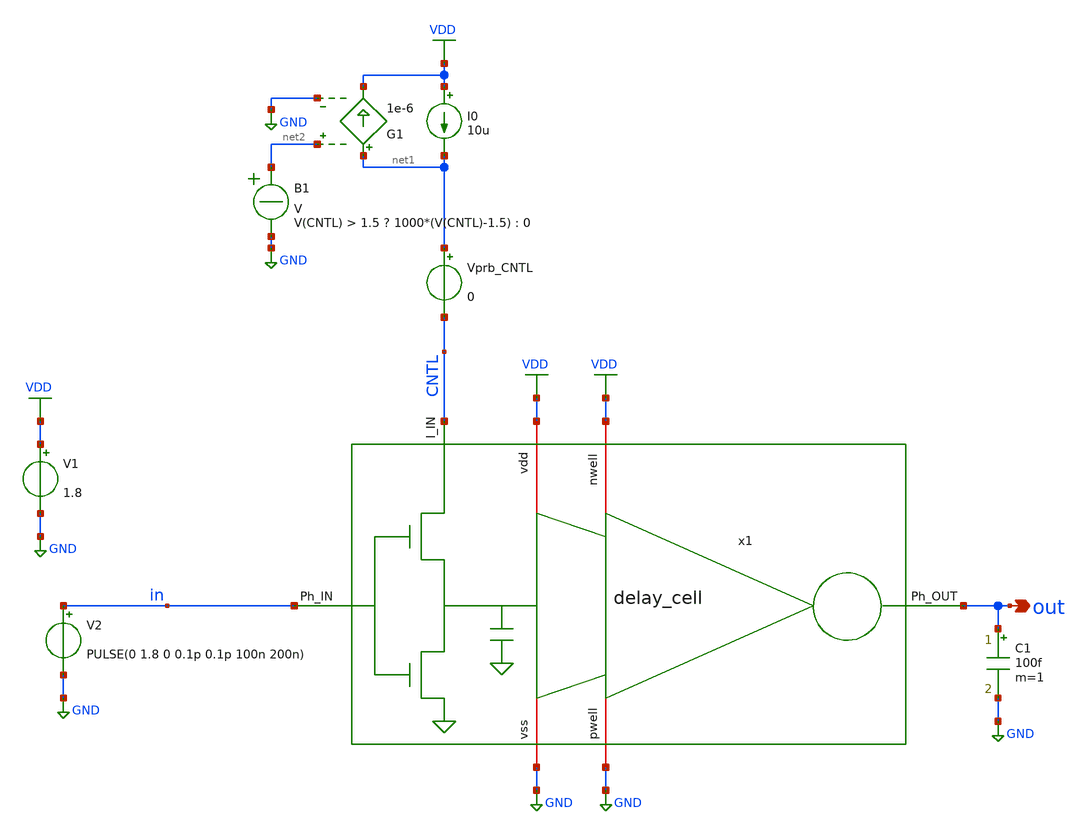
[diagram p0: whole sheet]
** sch_path: design/test/delaycell_test.sch
**.subckt delaycell_test out
*.opin out
V1 VDD GND 1.8
V2 in GND PULSE(0 1.8 0 0.1p 0.1p 100n 200n)
C1 out GND 100f m=1
I0 VDD net1 10u
x1 CNTL VDD VDD GND GND in out delay_cell
G1 net1 VDD net2 GND 1e-6
B1 net2 GND V = V(CNTL) > 1.5 ? 1000*(V(CNTL)-1.5) : 0
Vprb_CNTL net1 CNTL 0
**** begin user architecture code


.param temp=27



*.op
*.ac dec 10 1 10G
*.tran 0.01n 5u


.save all




.options wnflag=1
.include $::SKYWATER_MODELS/cells/nfet_01v8/sky130_fd_pr__nfet_01v8__tt.corner.spice
.include $::SKYWATER_MODELS/cells/nfet_01v8_lvt/sky130_fd_pr__nfet_01v8_lvt__tt.corner.spice
.include $::SKYWATER_MODELS/cells/pfet_01v8/sky130_fd_pr__pfet_01v8__tt.corner.spice
*.include $::SKYWATER_MODELS/cells/nfet_03v3_nvt/sky130_fd_pr__nfet_03v3_nvt__tt.corner.spice
*.include $::SKYWATER_MODELS/cells/nfet_05v0_nvt/sky130_fd_pr__nfet_05v0_nvt__tt.corner.spice
.include $::SKYWATER_MODELS/cells/esd_nfet_01v8/sky130_fd_pr__esd_nfet_01v8__tt.corner.spice
.include $::SKYWATER_MODELS/cells/pfet_01v8_lvt/sky130_fd_pr__pfet_01v8_lvt__tt.corner.spice
*.include $::SKYWATER_MODELS/cells/pfet_01v8_hvt/sky130_fd_pr__pfet_01v8_hvt__tt.corner.spice
*.include $::SKYWATER_MODELS/cells/esd_pfet_g5v0d10v5/sky130_fd_pr__esd_pfet_g5v0d10v5__tt.corner.spice
*.include $::SKYWATER_MODELS/cells/pfet_g5v0d10v5/sky130_fd_pr__pfet_g5v0d10v5__tt.corner.spice
*.include $::SKYWATER_MODELS/cells/pfet_g5v0d16v0/sky130_fd_pr__pfet_g5v0d16v0__tt.corner.spice
*.include $::SKYWATER_MODELS/cells/nfet_g5v0d10v5/sky130_fd_pr__nfet_g5v0d10v5__tt.corner.spice
*.include $::SKYWATER_MODELS/cells/nfet_g5v0d16v0/sky130_fd_pr__nfet_g5v0d16v0__tt_discrete.corner.spice
*.include $::SKYWATER_MODELS/cells/esd_nfet_g5v0d10v5/sky130_fd_pr__esd_nfet_g5v0d10v5__tt.corner.spice
.include $::SKYWATER_MODELS/models/corners/tt/nonfet.spice
* Mismatch parameters
.include $::SKYWATER_MODELS/cells/nfet_01v8/sky130_fd_pr__nfet_01v8__mismatch.corner.spice
.include $::SKYWATER_MODELS/cells/pfet_01v8/sky130_fd_pr__pfet_01v8__mismatch.corner.spice
.include $::SKYWATER_MODELS/cells/nfet_01v8_lvt/sky130_fd_pr__nfet_01v8_lvt__mismatch.corner.spice
.include $::SKYWATER_MODELS/cells/pfet_01v8_lvt/sky130_fd_pr__pfet_01v8_lvt__mismatch.corner.spice
*.include $::SKYWATER_MODELS/cells/pfet_01v8_hvt/sky130_fd_pr__pfet_01v8_hvt__mismatch.corner.spice
*.include $::SKYWATER_MODELS/cells/nfet_g5v0d10v5/sky130_fd_pr__nfet_g5v0d10v5__mismatch.corner.spice
*.include $::SKYWATER_MODELS/cells/pfet_g5v0d10v5/sky130_fd_pr__pfet_g5v0d10v5__mismatch.corner.spice
*.include $::SKYWATER_MODELS/cells/nfet_05v0_nvt/sky130_fd_pr__nfet_05v0_nvt__mismatch.corner.spice
*.include $::SKYWATER_MODELS/cells/nfet_03v3_nvt/sky130_fd_pr__nfet_03v3_nvt__mismatch.corner.spice
* Resistor$::SKYWATER_MODELS/Capacitor
.include $::SKYWATER_MODELS/models/r+c/res_typical__cap_typical.spice
.include $::SKYWATER_MODELS/models/r+c/res_typical__cap_typical__lin.spice
* Special cells
*.include $::SKYWATER_MODELS/models/corners/tt/specialized_cells.spice
* All models
.include $::SKYWATER_MODELS/models/all.spice
* Corner
.include $::SKYWATER_MODELS/models/corners/tt/rf.spice

* Manually adding standard cell models
.include /pdk/open_pdks/install/share/pdk/sky130A/libs.ref/sky130_fd_sc_hs/spice/sky130_fd_sc_hs.spice

**** end user architecture code
**.ends

* expanding   symbol:  core/delay_cell/delay_cell.sym # of pins=7
** sym_path: design/core/delay_cell/delay_cell.sym
** sch_path: design/core/delay_cell/delay_cell.sch
.subckt delay_cell I_IN nwell vdd pwell vss Ph_IN Ph_OUT
*.iopin vdd
*.iopin vss
*.iopin nwell
*.iopin pwell
*.opin Ph_OUT
*.ipin I_IN
*.ipin Ph_IN
XM_PA Va Ph_IN net1 nwell sky130_fd_pr__pfet_01v8 L=L_A W=W_PA nf=1 ad='int((nf+1)/2) * W/nf * 0.29'
+ as='int((nf+2)/2) * W/nf * 0.29' pd='2*int((nf+1)/2) * (W/nf + 0.29)' ps='2*int((nf+2)/2) * (W/nf + 0.29)'
+ nrd='0.29 / W' nrs='0.29 / W' sa=0 sb=0 sd=0 mult=1 m=1
XM_NA Va Ph_IN vss pwell sky130_fd_pr__nfet_01v8 L=L_A W=W_NA nf=1 ad='int((nf+1)/2) * W/nf * 0.29' as='int((nf+2)/2) * W/nf * 0.29'
+ pd='2*int((nf+1)/2) * (W/nf + 0.29)' ps='2*int((nf+2)/2) * (W/nf + 0.29)' nrd='0.29 / W' nrs='0.29 / W'
+ sa=0 sb=0 sd=0 mult=1 m=1
XM_SW net1 Ph_OUT I_IN nwell sky130_fd_pr__pfet_01v8 L=L_A W=W_SW nf=1 ad='int((nf+1)/2) * W/nf * 0.29'
+ as='int((nf+2)/2) * W/nf * 0.29' pd='2*int((nf+1)/2) * (W/nf + 0.29)' ps='2*int((nf+2)/2) * (W/nf + 0.29)'
+ nrd='0.29 / W' nrs='0.29 / W' sa=0 sb=0 sd=0 mult=1 m=1
XM_FB Va Vb vdd nwell sky130_fd_pr__pfet_01v8 L=L_A W=W_FB nf=1 ad='int((nf+1)/2) * W/nf * 0.29' as='int((nf+2)/2) * W/nf * 0.29'
+ pd='2*int((nf+1)/2) * (W/nf + 0.29)' ps='2*int((nf+2)/2) * (W/nf + 0.29)' nrd='0.29 / W' nrs='0.29 / W'
+ sa=0 sb=0 sd=0 mult=1 m=1
x_M_B vdd nwell Vb Va pwell vss sqar_inv W_CN=1 W_CP=1 L_SQ=1
x_M_C vdd nwell Ph_OUT Vb pwell vss sqar_inv W_CN=1 W_CP=1 L_SQ=1
.ends


* expanding   symbol:  core/sqar_inv/sqar_inv.sym # of pins=6
** sym_path: design/core/sqar_inv/sqar_inv.sym
** sch_path: design/core/sqar_inv/sqar_inv.sch
.subckt sqar_inv vdd nwell OUT IN pwell vss  W_CN=1 W_CP=1 L_SQ=1
*.ipin IN
*.opin OUT
*.iopin nwell
*.iopin pwell
*.iopin vss
*.iopin vdd
XM1 OUT IN vss pwell sky130_fd_pr__nfet_01v8 L=L_SQ W=W_CN nf=1 ad='int((nf+1)/2) * W/nf * 0.29' as='int((nf+2)/2) * W/nf * 0.29'
+ pd='2*int((nf+1)/2) * (W/nf + 0.29)' ps='2*int((nf+2)/2) * (W/nf + 0.29)' nrd='0.29 / W' nrs='0.29 / W'
+ sa=0 sb=0 sd=0 mult=1 m=1
XM2 OUT IN vdd nwell sky130_fd_pr__pfet_01v8 L=L_SQ W=W_CP nf=1 ad='int((nf+1)/2) * W/nf * 0.29' as='int((nf+2)/2) * W/nf * 0.29'
+ pd='2*int((nf+1)/2) * (W/nf + 0.29)' ps='2*int((nf+2)/2) * (W/nf + 0.29)' nrd='0.29 / W' nrs='0.29 / W'
+ sa=0 sb=0 sd=0 mult=1 m=1
.ends

.GLOBAL VDD
.GLOBAL GND
.end
